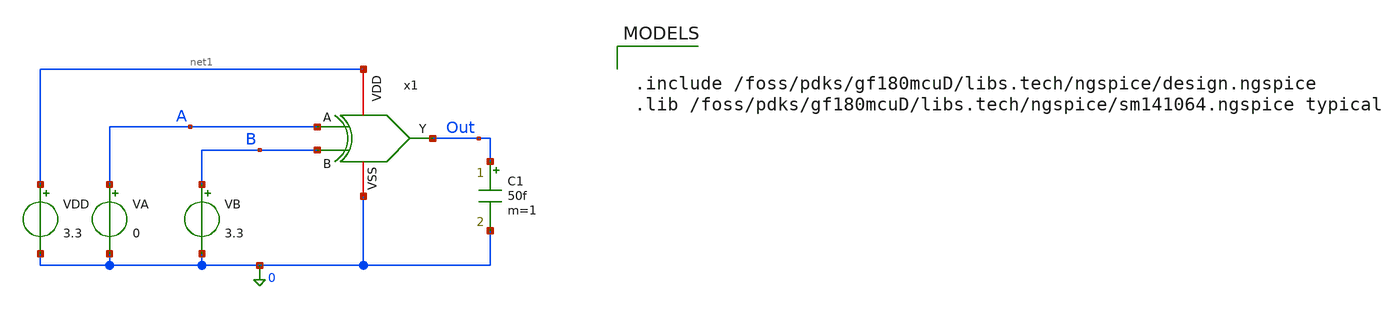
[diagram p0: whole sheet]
** sch_path: src/UN_PFD_GF180mcuD/work/UN_xor_0_gf180mcuD_TB.sch
* src/UN_PFD_GF180mcuD/work/UN_xor_0_gf180mcuD.sch:
* Copyright (C) 1998-2024 Stefan Frederik Schippers
* This program is free software; you can redistribute it and/or modify
* it under the terms of the GNU General Public License as published by
* the Free Software Foundation; either version 2 of the License, or
* (at your option) any later version.
**.subckt UN_xor_0_gf180mcuD_TB
VA A 0 0
VB B 0 3.3
C1 Out 0 50f m=1
VDD net1 0 3.3
x1 net1 A Out B 0 UN_xor_0_gf180mcuD
**** begin user architecture code



.control
save all *TODO: find out what this does.
set filetype=ascii

** Define Input Signal Properties.
** let allows calculations. set does not.

let fsig = 0.1e8
let tper = 1/fsig
let tfr = 0.01*tper
let ton = 0.5*tper-2*tfr
let tdel= 0.2*tper

** Define the parameters for Transient Analysis
** For transient Analysis, you have 2 parameters typically, How long to run sim and step size.

let tstop = 5*tper
let tstep = 0.001*tper

** Set the input sources with these parameters.
** VDD is already stable, but you can choose to simulate it separately.
** You use alter command to edit the default properties of the sources

alter @VA[DC] = 0.0
alter @VB[DC] = 3.3
alter @VA[PULSE] = [ 0 3.3 0 $&tfr $&tfr $&ton $&tper ]
alter @VB[PULSE] = [ 0 3.3 $&tdel $&tfr $&tfr $&ton $&tper ]

**** list of simulations to perform
**** The $& evaluates expressions and converts results to string because parameters are expected to
*+ be string

op
tran $&tstep $&tstop

** plots
setplot tran1
let vout = v(out)
let va= v(a)
let vb= v(b)

let ivdd = vdd#branch *1e3 * -1

plot vout va vb

setplot op1

write /foss/designs/un_basicpll_gf180mcud/un_pfd_gf180mcud/sim/xor_tb.raw tran1.all

.endc



.include /foss/pdks/gf180mcuD/libs.tech/ngspice/design.ngspice
.lib /foss/pdks/gf180mcuD/libs.tech/ngspice/sm141064.ngspice typical

**** end user architecture code
**.ends

* expanding   symbol:
*+  /foss/designs/UN_BasicPLL_GF180mcuD/UN_PFD_GF180mcuD/work/UN_xor_0_gf180mcuD.sym # of pins=5
** sym_path: src/UN_PFD_GF180mcuD/work/UN_xor_0_gf180mcuD.sym
** sch_path: src/UN_PFD_GF180mcuD/work/UN_xor_0_gf180mcuD.sch
.subckt UN_xor_0_gf180mcuD VDD A Y B VSS
*.iopin VSS
*.iopin VDD
*.opin Y
*.ipin A
*.ipin B
XM1 Y A_n net2 VSS nfet_03v3 L=0.28u W=0.5u nf=1 ad='int((nf+1)/2) * W/nf * 0.18u' as='int((nf+2)/2) * W/nf * 0.18u'
+ pd='2*int((nf+1)/2) * (W/nf + 0.18u)' ps='2*int((nf+2)/2) * (W/nf + 0.18u)' nrd='0.18u / W' nrs='0.18u / W'
+ sa=0 sb=0 sd=0 m=1
XM2 Y A net1 VSS nfet_03v3 L=0.28u W=0.5u nf=1 ad='int((nf+1)/2) * W/nf * 0.18u' as='int((nf+2)/2) * W/nf * 0.18u'
+ pd='2*int((nf+1)/2) * (W/nf + 0.18u)' ps='2*int((nf+2)/2) * (W/nf + 0.18u)' nrd='0.18u / W' nrs='0.18u / W'
+ sa=0 sb=0 sd=0 m=1
XM3 net2 B_n VSS VSS nfet_03v3 L=0.28u W=0.5u nf=1 ad='int((nf+1)/2) * W/nf * 0.18u' as='int((nf+2)/2) * W/nf * 0.18u'
+ pd='2*int((nf+1)/2) * (W/nf + 0.18u)' ps='2*int((nf+2)/2) * (W/nf + 0.18u)' nrd='0.18u / W' nrs='0.18u / W'
+ sa=0 sb=0 sd=0 m=1
XM4 net1 B VSS VSS nfet_03v3 L=0.28u W=0.5u nf=1 ad='int((nf+1)/2) * W/nf * 0.18u' as='int((nf+2)/2) * W/nf * 0.18u'
+ pd='2*int((nf+1)/2) * (W/nf + 0.18u)' ps='2*int((nf+2)/2) * (W/nf + 0.18u)' nrd='0.18u / W' nrs='0.18u / W'
+ sa=0 sb=0 sd=0 m=1
XM5 Y A_n net3 VDD pfet_03v3 L=0.28u W=1u nf=1 ad='int((nf+1)/2) * W/nf * 0.18u' as='int((nf+2)/2) * W/nf * 0.18u'
+ pd='2*int((nf+1)/2) * (W/nf + 0.18u)' ps='2*int((nf+2)/2) * (W/nf + 0.18u)' nrd='0.18u / W' nrs='0.18u / W'
+ sa=0 sb=0 sd=0 m=1
XM6 net3 A VDD VDD pfet_03v3 L=0.28u W=1u nf=1 ad='int((nf+1)/2) * W/nf * 0.18u' as='int((nf+2)/2) * W/nf * 0.18u'
+ pd='2*int((nf+1)/2) * (W/nf + 0.18u)' ps='2*int((nf+2)/2) * (W/nf + 0.18u)' nrd='0.18u / W' nrs='0.18u / W'
+ sa=0 sb=0 sd=0 m=1
XM7 Y B_n net4 VDD pfet_03v3 L=0.28u W=1u nf=1 ad='int((nf+1)/2) * W/nf * 0.18u' as='int((nf+2)/2) * W/nf * 0.18u'
+ pd='2*int((nf+1)/2) * (W/nf + 0.18u)' ps='2*int((nf+2)/2) * (W/nf + 0.18u)' nrd='0.18u / W' nrs='0.18u / W'
+ sa=0 sb=0 sd=0 m=1
XM8 net4 B VDD VDD pfet_03v3 L=0.28u W=1u nf=1 ad='int((nf+1)/2) * W/nf * 0.18u' as='int((nf+2)/2) * W/nf * 0.18u'
+ pd='2*int((nf+1)/2) * (W/nf + 0.18u)' ps='2*int((nf+2)/2) * (W/nf + 0.18u)' nrd='0.18u / W' nrs='0.18u / W'
+ sa=0 sb=0 sd=0 m=1
XM9 A_n A VDD VDD pfet_03v3 L=0.28u W=1u nf=1 ad='int((nf+1)/2) * W/nf * 0.18u' as='int((nf+2)/2) * W/nf * 0.18u'
+ pd='2*int((nf+1)/2) * (W/nf + 0.18u)' ps='2*int((nf+2)/2) * (W/nf + 0.18u)' nrd='0.18u / W' nrs='0.18u / W'
+ sa=0 sb=0 sd=0 m=1
XM10 A_n A VSS VSS nfet_03v3 L=0.28u W=0.5u nf=1 ad='int((nf+1)/2) * W/nf * 0.18u' as='int((nf+2)/2) * W/nf * 0.18u'
+ pd='2*int((nf+1)/2) * (W/nf + 0.18u)' ps='2*int((nf+2)/2) * (W/nf + 0.18u)' nrd='0.18u / W' nrs='0.18u / W'
+ sa=0 sb=0 sd=0 m=1
XM11 B_n B VDD VDD pfet_03v3 L=0.28u W=1u nf=1 ad='int((nf+1)/2) * W/nf * 0.18u' as='int((nf+2)/2) * W/nf * 0.18u'
+ pd='2*int((nf+1)/2) * (W/nf + 0.18u)' ps='2*int((nf+2)/2) * (W/nf + 0.18u)' nrd='0.18u / W' nrs='0.18u / W'
+ sa=0 sb=0 sd=0 m=1
XM12 B_n B VSS VSS nfet_03v3 L=0.28u W=0.5u nf=1 ad='int((nf+1)/2) * W/nf * 0.18u' as='int((nf+2)/2) * W/nf * 0.18u'
+ pd='2*int((nf+1)/2) * (W/nf + 0.18u)' ps='2*int((nf+2)/2) * (W/nf + 0.18u)' nrd='0.18u / W' nrs='0.18u / W'
+ sa=0 sb=0 sd=0 m=1
.ends

.end
